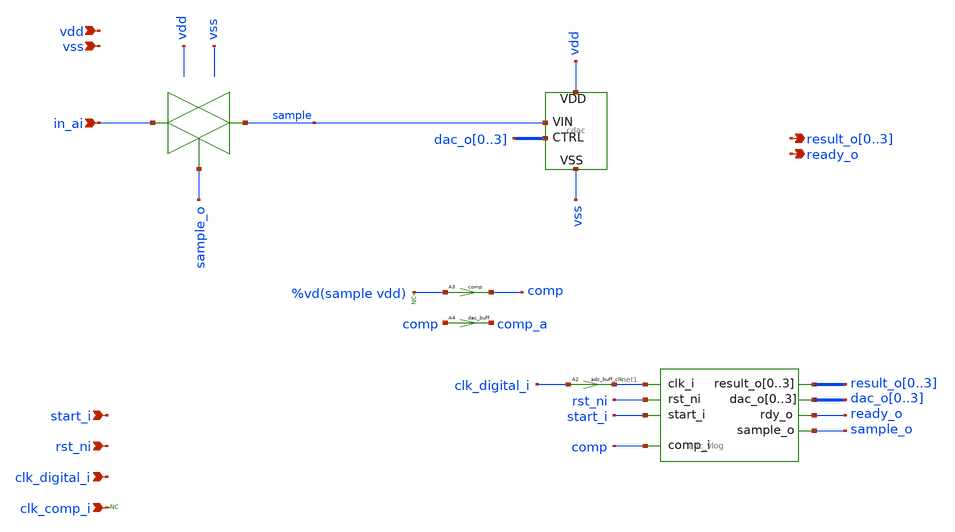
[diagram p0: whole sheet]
** sch_path: designs/basic1/adc.sch
* IHP-GmbH/IHP-Open-PDK/ihp-sg13g2/libs.tech/xschem/sg13g2_stdcells/sg13g2_inv_2.sch:
* Copyright 2023 IHP PDK Authors
* Licensed under the Apache License, Version 2.0 (the "License");
**.subckt adc in_ai clk_digital_i vss vdd rst_ni start_i ready_o
*+ result_o0,result_o1,result_o2,result_o3 clk_comp_i
*.ipin in_ai
*.ipin clk_digital_i
*.ipin vss
*.ipin vdd
*.ipin rst_ni
*.ipin start_i
*.opin ready_o
*.opin result_o0,result_o1,result_o2,result_o3
*.ipin clk_comp_i
x3 sample dac_o0 dac_o1 dac_o2 dac_o3 dac_o0 dac_o1 dac_o2 dac_o3 vss vdd cdac
A2 [ clk_digital_i ] [ net1 ] adc_buff_clk
A1 [ net1 start_i rst_ni comp ] [ ready_o sample_o dac_o0 dac_o1 dac_o2 dac_o3 result_o0 result_o1
+ result_o2 result_o3 ] adc
A3 [ %vd(sample vdd) ] [ comp ] comp
A4 [ comp ] [ comp_a ] dac_buff
* noconn %vd(sample vdd)
* noconn clk_comp_i
**.ends

* expanding   symbol:  /workspaces/ngspice_cosim_inv/designs/cdac/cdac.sym # of pins=4
** sym_path: designs/cdac/cdac.sym
** sch_path: designs/cdac/cdac.sch
.subckt cdac VIN CTRL0 CTRL1 CTRL2 CTRL3 CTRL4 CTRL5 CTRL6 CTRL7 VSS VDD
*.ipin VIN
*.ipin CTRL0,CTRL1,CTRL2,CTRL3,CTRL4,CTRL5,CTRL6,CTRL7
*.ipin VSS
*.ipin VDD
XC2 VIN l1 cap_cmim w=7.297e-5 l=7.298e-5 m=1 mm_ok=1
XC3 VIN l2 cap_cmim w=5.158e-5 l=5.159e-5 m=1 mm_ok=1
XC4 VIN l3 cap_cmim w=3.646e-5 l=3.646e-5 m=1 mm_ok=1
XC5 VIN VSS cap_cmim w=6.402e-6 l=6.402e-6 m=1 mm_ok=1
x1 l1 CTRL0 VDD VSS sg13g2_inv_2
x2 l2 CTRL1 VDD VSS sg13g2_inv_2
x3 l3 CTRL2 VDD VSS sg13g2_inv_2
x4 l4 CTRL3 VDD VSS sg13g2_inv_2
XC6 VIN l4 cap_cmim w=2.577e-5 l=2.577e-5 m=1 mm_ok=1
XC7 VIN l5 cap_cmim w=1.820e-5 l=1.820e-5 m=1 mm_ok=1
XC8 VIN l6 cap_cmim w=1.286e-5 l=1.286e-5 m=1 mm_ok=1
XC9 VIN l7 cap_cmim w=9.077e-6 l=9.077e-6 m=1 mm_ok=1
x5 l5 CTRL4 VDD VSS sg13g2_inv_2
x6 l6 CTRL5 VDD VSS sg13g2_inv_2
x7 l7 CTRL6 VDD VSS sg13g2_inv_2
x8 l8 CTRL7 VDD VSS sg13g2_inv_2
XC1 VIN l8 cap_cmim w=6.402e-6 l=6.402e-6 m=1 mm_ok=1
.ends


* expanding   symbol:  sg13g2_stdcells/sg13g2_inv_2.sym # of pins=2
** sym_path: sg13g2_stdcells/sg13g2_inv_2.sym
** sch_path: sg13g2_stdcells/sg13g2_inv_2.sch
.subckt sg13g2_inv_2 Y A VDD VSS
*.opin Y
*.ipin A
*.iopin VDD
*.iopin VSS
XM1 Y A VSS VSS sg13_lv_nmos w=1.48u l=130.00n ng=2 m=1 mm_ok=1
XM2 Y A VDD VDD sg13_lv_pmos w=2.24u l=130.00n ng=2 m=1 mm_ok=1
.ends

**** begin user architecture code
.model adc d_cosim simulation="ivlng" sim_args=["adc"]
.model dac_buff dac_bridge input_load=1e-15 t_rise=10n t_fall=10n  out_low=0 out_high=1.5
.model comp adc_bridge in_low=0 in_high=0
**** end user architecture code
.end
